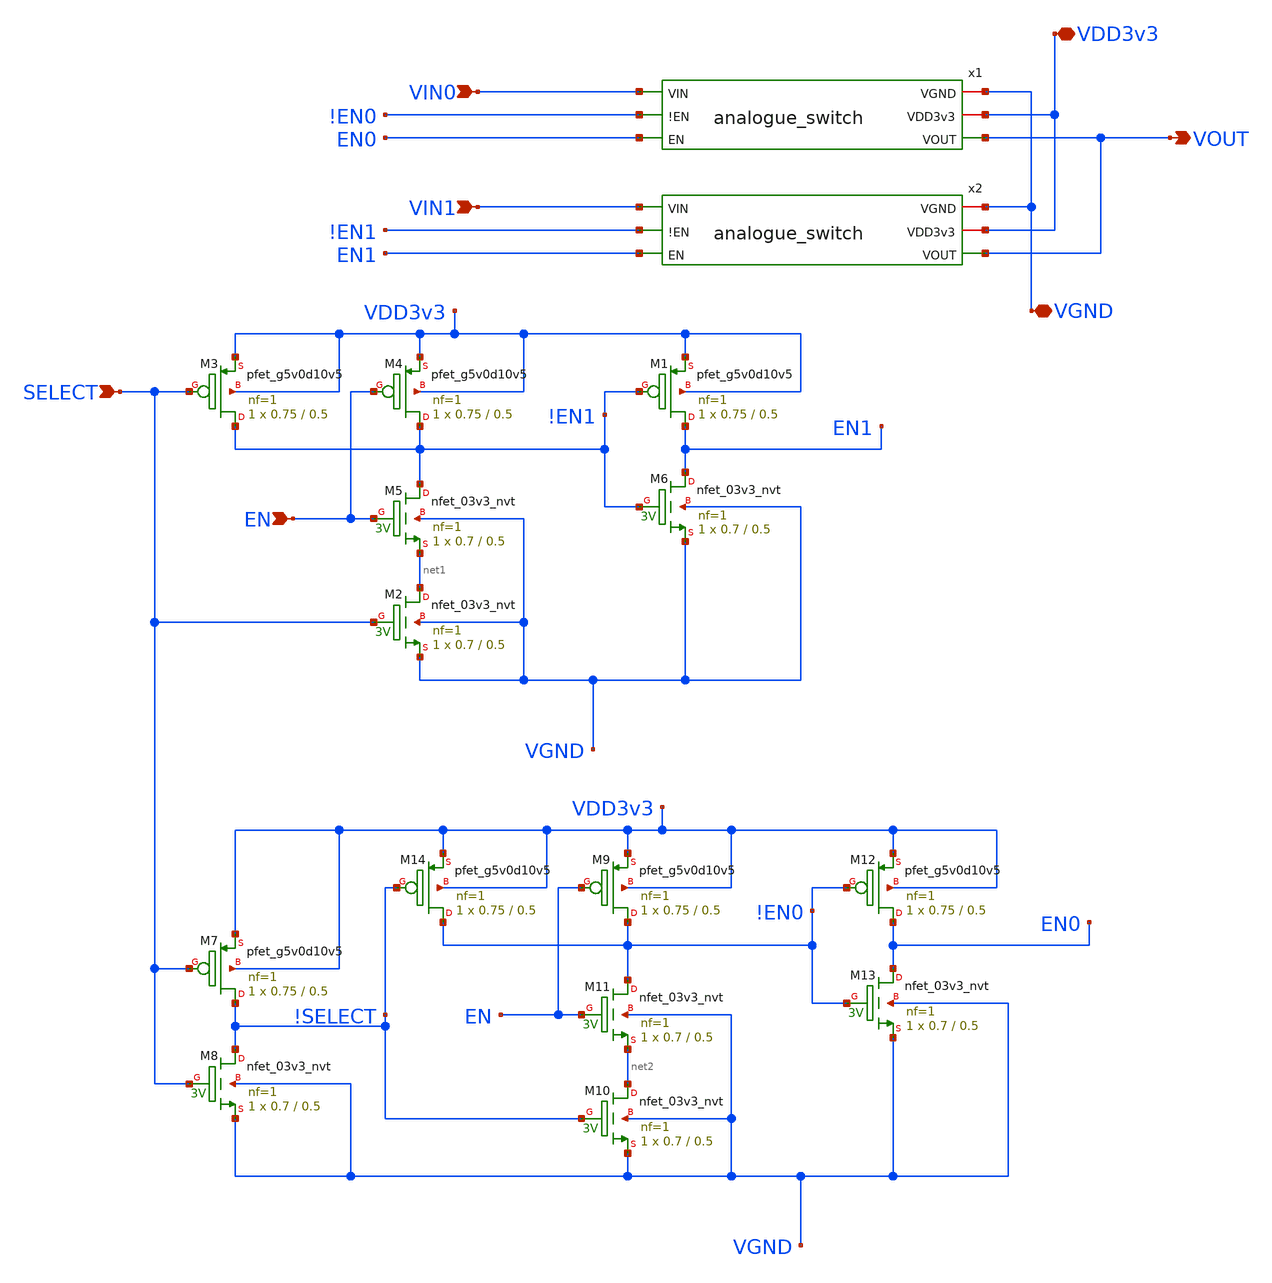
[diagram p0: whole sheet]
** sch_path: xschem/analog_mux_2_1.sch
**.subckt analog_mux_2_1 VGND VIN0 VOUT VDD3v3 VIN1 EN SELECT
*.iopin VGND
*.ipin VIN0
*.opin VOUT
*.iopin VDD3v3
*.ipin VIN1
*.ipin EN
*.ipin SELECT
x1 VIN0 VGND VDD3v3 !EN0 EN0 VOUT analogue_switch
x2 VIN1 VGND VDD3v3 !EN1 EN1 VOUT analogue_switch
XM3 !EN1 SELECT VDD3v3 VDD3v3 sky130_fd_pr__pfet_g5v0d10v5 L=0.5 W=0.75 nf=1 ad='int((nf+1)/2) * W/nf * 0.29'
+ as='int((nf+2)/2) * W/nf * 0.29' pd='2*int((nf+1)/2) * (W/nf + 0.29)' ps='2*int((nf+2)/2) * (W/nf + 0.29)'
+ nrd='0.29 / W' nrs='0.29 / W' sa=0 sb=0 sd=0 mult=1 m=1
XM4 !EN1 EN VDD3v3 VDD3v3 sky130_fd_pr__pfet_g5v0d10v5 L=0.5 W=0.75 nf=1 ad='int((nf+1)/2) * W/nf * 0.29'
+ as='int((nf+2)/2) * W/nf * 0.29' pd='2*int((nf+1)/2) * (W/nf + 0.29)' ps='2*int((nf+2)/2) * (W/nf + 0.29)'
+ nrd='0.29 / W' nrs='0.29 / W' sa=0 sb=0 sd=0 mult=1 m=1
XM2 net1 SELECT VGND VGND sky130_fd_pr__nfet_03v3_nvt L=0.5 W=0.7 nf=1 ad='int((nf+1)/2) * W/nf * 0.29'
+ as='int((nf+2)/2) * W/nf * 0.29' pd='2*int((nf+1)/2) * (W/nf + 0.29)' ps='2*int((nf+2)/2) * (W/nf + 0.29)'
+ nrd='0.29 / W' nrs='0.29 / W' sa=0 sb=0 sd=0 mult=1 m=1
XM5 !EN1 EN net1 VGND sky130_fd_pr__nfet_03v3_nvt L=0.5 W=0.7 nf=1 ad='int((nf+1)/2) * W/nf * 0.29' as='int((nf+2)/2) * W/nf * 0.29'
+ pd='2*int((nf+1)/2) * (W/nf + 0.29)' ps='2*int((nf+2)/2) * (W/nf + 0.29)' nrd='0.29 / W' nrs='0.29 / W'
+ sa=0 sb=0 sd=0 mult=1 m=1
XM1 EN1 !EN1 VDD3v3 VDD3v3 sky130_fd_pr__pfet_g5v0d10v5 L=0.5 W=0.75 nf=1 ad='int((nf+1)/2) * W/nf * 0.29'
+ as='int((nf+2)/2) * W/nf * 0.29' pd='2*int((nf+1)/2) * (W/nf + 0.29)' ps='2*int((nf+2)/2) * (W/nf + 0.29)'
+ nrd='0.29 / W' nrs='0.29 / W' sa=0 sb=0 sd=0 mult=1 m=1
XM6 EN1 !EN1 VGND VGND sky130_fd_pr__nfet_03v3_nvt L=0.5 W=0.7 nf=1 ad='int((nf+1)/2) * W/nf * 0.29'
+ as='int((nf+2)/2) * W/nf * 0.29' pd='2*int((nf+1)/2) * (W/nf + 0.29)' ps='2*int((nf+2)/2) * (W/nf + 0.29)'
+ nrd='0.29 / W' nrs='0.29 / W' sa=0 sb=0 sd=0 mult=1 m=1
XM7 !SELECT SELECT VDD3v3 VDD3v3 sky130_fd_pr__pfet_g5v0d10v5 L=0.5 W=0.75 nf=1 ad='int((nf+1)/2) * W/nf * 0.29'
+ as='int((nf+2)/2) * W/nf * 0.29' pd='2*int((nf+1)/2) * (W/nf + 0.29)' ps='2*int((nf+2)/2) * (W/nf + 0.29)'
+ nrd='0.29 / W' nrs='0.29 / W' sa=0 sb=0 sd=0 mult=1 m=1
XM8 !SELECT SELECT VGND VGND sky130_fd_pr__nfet_03v3_nvt L=0.5 W=0.7 nf=1 ad='int((nf+1)/2) * W/nf * 0.29'
+ as='int((nf+2)/2) * W/nf * 0.29' pd='2*int((nf+1)/2) * (W/nf + 0.29)' ps='2*int((nf+2)/2) * (W/nf + 0.29)'
+ nrd='0.29 / W' nrs='0.29 / W' sa=0 sb=0 sd=0 mult=1 m=1
XM9 !EN0 EN VDD3v3 VDD3v3 sky130_fd_pr__pfet_g5v0d10v5 L=0.5 W=0.75 nf=1 ad='int((nf+1)/2) * W/nf * 0.29'
+ as='int((nf+2)/2) * W/nf * 0.29' pd='2*int((nf+1)/2) * (W/nf + 0.29)' ps='2*int((nf+2)/2) * (W/nf + 0.29)'
+ nrd='0.29 / W' nrs='0.29 / W' sa=0 sb=0 sd=0 mult=1 m=1
XM10 net2 !SELECT VGND VGND sky130_fd_pr__nfet_03v3_nvt L=0.5 W=0.7 nf=1 ad='int((nf+1)/2) * W/nf * 0.29'
+ as='int((nf+2)/2) * W/nf * 0.29' pd='2*int((nf+1)/2) * (W/nf + 0.29)' ps='2*int((nf+2)/2) * (W/nf + 0.29)'
+ nrd='0.29 / W' nrs='0.29 / W' sa=0 sb=0 sd=0 mult=1 m=1
XM11 !EN0 EN net2 VGND sky130_fd_pr__nfet_03v3_nvt L=0.5 W=0.7 nf=1 ad='int((nf+1)/2) * W/nf * 0.29'
+ as='int((nf+2)/2) * W/nf * 0.29' pd='2*int((nf+1)/2) * (W/nf + 0.29)' ps='2*int((nf+2)/2) * (W/nf + 0.29)'
+ nrd='0.29 / W' nrs='0.29 / W' sa=0 sb=0 sd=0 mult=1 m=1
XM12 EN0 !EN0 VDD3v3 VDD3v3 sky130_fd_pr__pfet_g5v0d10v5 L=0.5 W=0.75 nf=1 ad='int((nf+1)/2) * W/nf * 0.29'
+ as='int((nf+2)/2) * W/nf * 0.29' pd='2*int((nf+1)/2) * (W/nf + 0.29)' ps='2*int((nf+2)/2) * (W/nf + 0.29)'
+ nrd='0.29 / W' nrs='0.29 / W' sa=0 sb=0 sd=0 mult=1 m=1
XM13 EN0 !EN0 VGND VGND sky130_fd_pr__nfet_03v3_nvt L=0.5 W=0.7 nf=1 ad='int((nf+1)/2) * W/nf * 0.29'
+ as='int((nf+2)/2) * W/nf * 0.29' pd='2*int((nf+1)/2) * (W/nf + 0.29)' ps='2*int((nf+2)/2) * (W/nf + 0.29)'
+ nrd='0.29 / W' nrs='0.29 / W' sa=0 sb=0 sd=0 mult=1 m=1
XM14 !EN0 !SELECT VDD3v3 VDD3v3 sky130_fd_pr__pfet_g5v0d10v5 L=0.5 W=0.75 nf=1 ad='int((nf+1)/2) * W/nf * 0.29'
+ as='int((nf+2)/2) * W/nf * 0.29' pd='2*int((nf+1)/2) * (W/nf + 0.29)' ps='2*int((nf+2)/2) * (W/nf + 0.29)'
+ nrd='0.29 / W' nrs='0.29 / W' sa=0 sb=0 sd=0 mult=1 m=1
**.ends

* expanding   symbol:  analogue_switch.sym # of pins=6
** sym_path: xschem/analogue_switch.sym
** sch_path: xschem/analogue_switch.sch
.subckt analogue_switch VIN VGND VDD3v3 !EN EN VOUT
*.iopin VGND
*.iopin VDD3v3
*.ipin EN
*.ipin VIN
*.ipin !EN
*.opin VOUT
XM2 VOUT !EN VIN VDD3v3 sky130_fd_pr__pfet_g5v0d10v5 L=0.5 W=1 nf=1 ad='int((nf+1)/2) * W/nf * 0.29'
+ as='int((nf+2)/2) * W/nf * 0.29' pd='2*int((nf+1)/2) * (W/nf + 0.29)' ps='2*int((nf+2)/2) * (W/nf + 0.29)'
+ nrd='0.29 / W' nrs='0.29 / W' sa=0 sb=0 sd=0 mult=15 m=15
XM1 VIN EN VOUT VGND sky130_fd_pr__nfet_03v3_nvt L=0.5 W=1 nf=1 ad='int((nf+1)/2) * W/nf * 0.29' as='int((nf+2)/2) * W/nf * 0.29'
+ pd='2*int((nf+1)/2) * (W/nf + 0.29)' ps='2*int((nf+2)/2) * (W/nf + 0.29)' nrd='0.29 / W' nrs='0.29 / W'
+ sa=0 sb=0 sd=0 mult=10 m=10
.ends

.end
